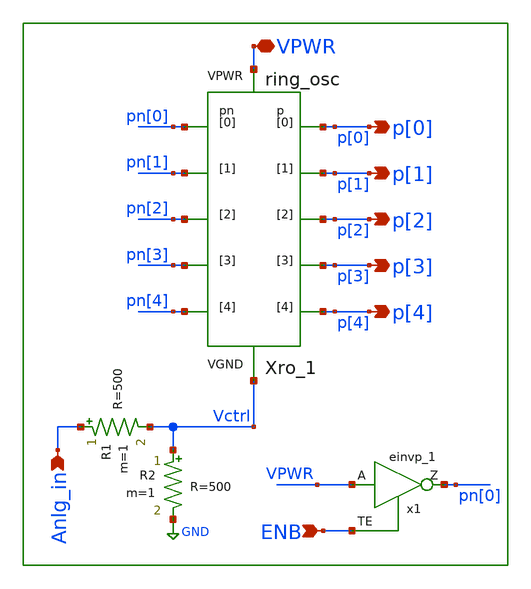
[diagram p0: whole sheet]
** sch_path: circuit_model/lib/vco.sch
**.subckt vco Anlg_in VPWR p[0] ENB p[1] p[2] p[3] p[4]
*.ipin Anlg_in
*.iopin VPWR
*.opin p[0]
*.ipin ENB
*.opin p[1]
*.opin p[2]
*.opin p[3]
*.opin p[4]
x1 VPWR ENB VGND VNB VPB VPWR pn[0] sky130_fd_sc_hd__einvp_1
Xro_1 Vctrl VPWR p[0] p[1] p[2] p[3] p[4] pn[0] pn[1] pn[2] pn[3] pn[4] ring_osc L12="L12"
+ Wp12="Wp12" Wn12="Wn12" L34="L34" Wp34="Wp34" Wn34="Wn34"
R2 Vctrl GND R=500 m=1
R1 Anlg_in Vctrl R=500 m=1
**.ends

* expanding   symbol:  ring_osc.sym # of pins=12
** sym_path: circuit_model/lib/ring_osc.sym
** sch_path: circuit_model/lib/ring_osc.sch
.subckt ring_osc VGND VPWR p[0] p[1] p[2] p[3] p[4] pn[0] pn[1] pn[2] pn[3] pn[4]  L12=0.15 Wp12=2.4
+ Wn12=1.2 L34=0.15 Wp34=1.2 Wn34=0.65
*.iopin VPWR
*.iopin VGND
*.opin pn[0]
*.iopin p[0]
*.opin pn[1]
*.opin p[1]
*.opin p[2]
*.opin p[3]
*.opin p[4]
*.opin pn[2]
*.opin pn[3]
*.opin pn[4]
Xi_1 p[4] pn[4] VPWR VGND p[0] pn[0] cc_inv L12="L12" Wp12="Wp12" Wn12="Wn12" L34="L34" Wp34="Wp34"
+ Wn34="Wn34"
Xi_2 p[0] pn[0] VPWR VGND p[1] pn[1] cc_inv L12="L12" Wp12="Wp12" Wn12="Wn12" L34="L34" Wp34="Wp34"
+ Wn34="Wn34"
Xi_3 p[1] pn[1] VPWR VGND p[2] pn[2] cc_inv L12="L12" Wp12="Wp12" Wn12="Wn12" L34="L34" Wp34="Wp34"
+ Wn34="Wn34"
Xi_4 p[2] pn[2] VPWR VGND p[3] pn[3] cc_inv L12="L12" Wp12="Wp12" Wn12="Wn12" L34="L34" Wp34="Wp34"
+ Wn34="Wn34"
Xi_5 p[3] pn[3] VPWR VGND p[4] pn[4] cc_inv L12="L12" Wp12="Wp12" Wn12="Wn12" L34="L34" Wp34="Wp34"
+ Wn34="Wn34"
.ends


* expanding   symbol:  cc_inv.sym # of pins=6
** sym_path: circuit_model/lib/cc_inv.sym
** sch_path: circuit_model/lib/cc_inv.sch
.subckt cc_inv inp inn VPWR VGND outp outn  L12=0.15 Wp12=1.2 Wn12=0.65 L34=0.15 Wp34=1.2 Wn34=0.65
*.opin outp
*.ipin inn
*.iopin VGND
*.opin outn
*.ipin inp
*.iopin VPWR
Xi_1 inp VPWR VGND outp inverter L="L12" Wp="Wp12" Np=1 Wn="Wn12" Nn=1
Xi_3 outp VPWR VGND outn inverter L="L34" Wp="Wp34" Np=1 Wn="Wn34" Nn=1
Xi_2 inn VPWR VGND outn inverter L="L12" Wp="Wp12" Np=1 Wn="Wn12" Nn=1
Xi_4 outn VPWR VGND outp inverter L="L34" Wp="Wp34" Np=1 Wn="Wn34" Nn=1
.ends


* expanding   symbol:  inverter.sym # of pins=4
** sym_path: circuit_model/lib/inverter.sym
** sch_path: circuit_model/lib/inverter.sch
.subckt inverter A VPWR VGND Y  L=0.15 Wp=1.2 Np=1 Wn=0.65 Nn=1
*.iopin VPWR
*.iopin VGND
*.ipin A
*.opin Y
XM1 Y A VPWR VDD sky130_fd_pr__pfet_01v8 L="L" W="Wp" nf="Np" ad='int(("Np" + 1)/2) * "Wp" / "Np" * 0.29'
+ as='int(("Np" + 2)/2) * "Wp" / "Np" * 0.29' pd='2*int(("Np" + 1)/2) * ("Wp" / "Np" + 0.29)' ps='2*int(("Np" + 2)/2) * ("Wp" / "Np" + 0.29)'
+ nrd='0.29 / "Wp" ' nrs='0.29 / "Wp" ' sa=0 sb=0 sd=0 mult=1 m=1
XM2 Y A VGND GND sky130_fd_pr__nfet_01v8 L="L" W="Wn" nf="Nn" ad='int((nf+1)/2) * W/nf * 0.29' as='int((nf+2)/2) * W/nf * 0.29'
+ pd='2*int((nf+1)/2) * (W/nf + 0.29)' ps='2*int((nf+2)/2) * (W/nf + 0.29)' nrd='0.29 / W' nrs='0.29 / W'
+ sa=0 sb=0 sd=0 mult=1 m=1
.ends

.GLOBAL GND
.end
